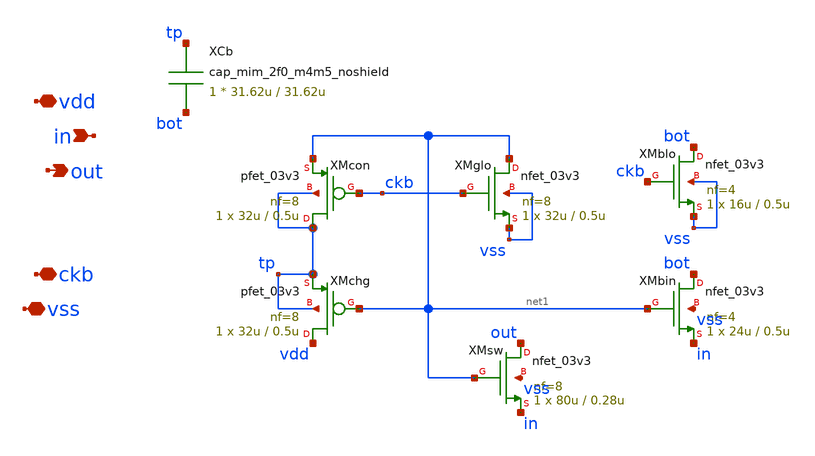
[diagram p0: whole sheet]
** sch_path: blocks/adc/comp-array/boot3.sch
**.subckt boot3 vdd in ckb vss out
*.iopin vdd
*.ipin in
*.iopin ckb
*.iopin vss
*.opin out
XMchg vdd net1 tp tp pfet_03v3 L=0.5u W=32u nf=8 ad='int((nf+1)/2) * W/nf * 0.18u' as='int((nf+2)/2) * W/nf * 0.18u'
+ pd='2*int((nf+1)/2) * (W/nf + 0.18u)' ps='2*int((nf+2)/2) * (W/nf + 0.18u)' nrd='0.18u / W' nrs='0.18u / W'
+ sa=0 sb=0 sd=0 m=1
XCb tp bot cap_mim_2f0_m4m5_noshield c_width=31.62u c_length=31.62u m=1
XMcon tp ckb net1 tp pfet_03v3 L=0.5u W=32u nf=8 ad='int((nf+1)/2) * W/nf * 0.18u' as='int((nf+2)/2) * W/nf * 0.18u'
+ pd='2*int((nf+1)/2) * (W/nf + 0.18u)' ps='2*int((nf+2)/2) * (W/nf + 0.18u)' nrd='0.18u / W' nrs='0.18u / W'
+ sa=0 sb=0 sd=0 m=1
XMglo net1 ckb vss vss nfet_03v3 L=0.5u W=32u nf=8 ad='int((nf+1)/2) * W/nf * 0.18u' as='int((nf+2)/2) * W/nf * 0.18u'
+ pd='2*int((nf+1)/2) * (W/nf + 0.18u)' ps='2*int((nf+2)/2) * (W/nf + 0.18u)' nrd='0.18u / W' nrs='0.18u / W'
+ sa=0 sb=0 sd=0 m=1
XMblo bot ckb vss vss nfet_03v3 L=0.5u W=16u nf=4 ad='int((nf+1)/2) * W/nf * 0.18u' as='int((nf+2)/2) * W/nf * 0.18u'
+ pd='2*int((nf+1)/2) * (W/nf + 0.18u)' ps='2*int((nf+2)/2) * (W/nf + 0.18u)' nrd='0.18u / W' nrs='0.18u / W'
+ sa=0 sb=0 sd=0 m=1
XMbin bot net1 in vss nfet_03v3 L=0.5u W=24u nf=4 ad='int((nf+1)/2) * W/nf * 0.18u' as='int((nf+2)/2) * W/nf * 0.18u'
+ pd='2*int((nf+1)/2) * (W/nf + 0.18u)' ps='2*int((nf+2)/2) * (W/nf + 0.18u)' nrd='0.18u / W' nrs='0.18u / W'
+ sa=0 sb=0 sd=0 m=1
XMsw out net1 in vss nfet_03v3 L=0.28u W=80u nf=8 ad='int((nf+1)/2) * W/nf * 0.18u' as='int((nf+2)/2) * W/nf * 0.18u'
+ pd='2*int((nf+1)/2) * (W/nf + 0.18u)' ps='2*int((nf+2)/2) * (W/nf + 0.18u)' nrd='0.18u / W' nrs='0.18u / W'
+ sa=0 sb=0 sd=0 m=1
**.ends
.end
